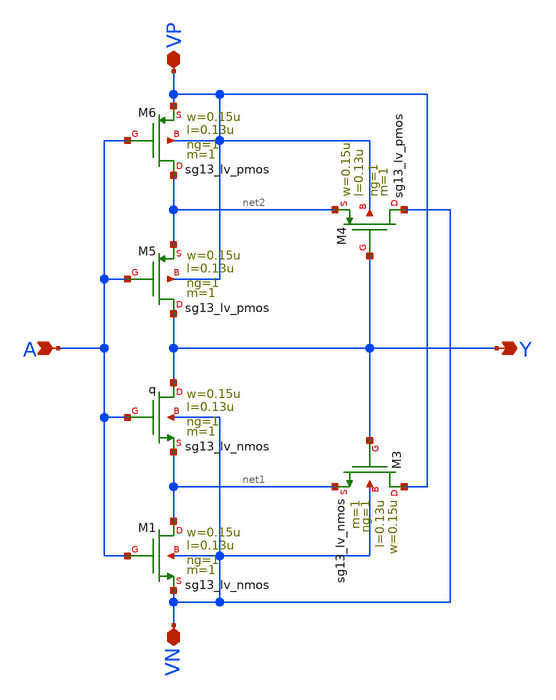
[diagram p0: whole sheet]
** sch_path: xschem/strig.sch
**.subckt strig VP VN A Y
*.iopin VP
*.iopin VN
*.ipin A
*.opin Y
XM1 net1 A VN VN sg13_lv_nmos w=0.15u l=0.13u ng=1 m=1 mm_ok=1
Xq Y A net1 VN sg13_lv_nmos w=0.15u l=0.13u ng=1 m=1 mm_ok=1
XM3 VP Y net1 VN sg13_lv_nmos w=0.15u l=0.13u ng=1 m=1 mm_ok=1
XM4 VN Y net2 VP sg13_lv_pmos w=0.15u l=0.13u ng=1 m=1 mm_ok=1
XM5 Y A net2 VP sg13_lv_pmos w=0.15u l=0.13u ng=1 m=1 mm_ok=1
XM6 net2 A VP VP sg13_lv_pmos w=0.15u l=0.13u ng=1 m=1 mm_ok=1
**.ends
.end
